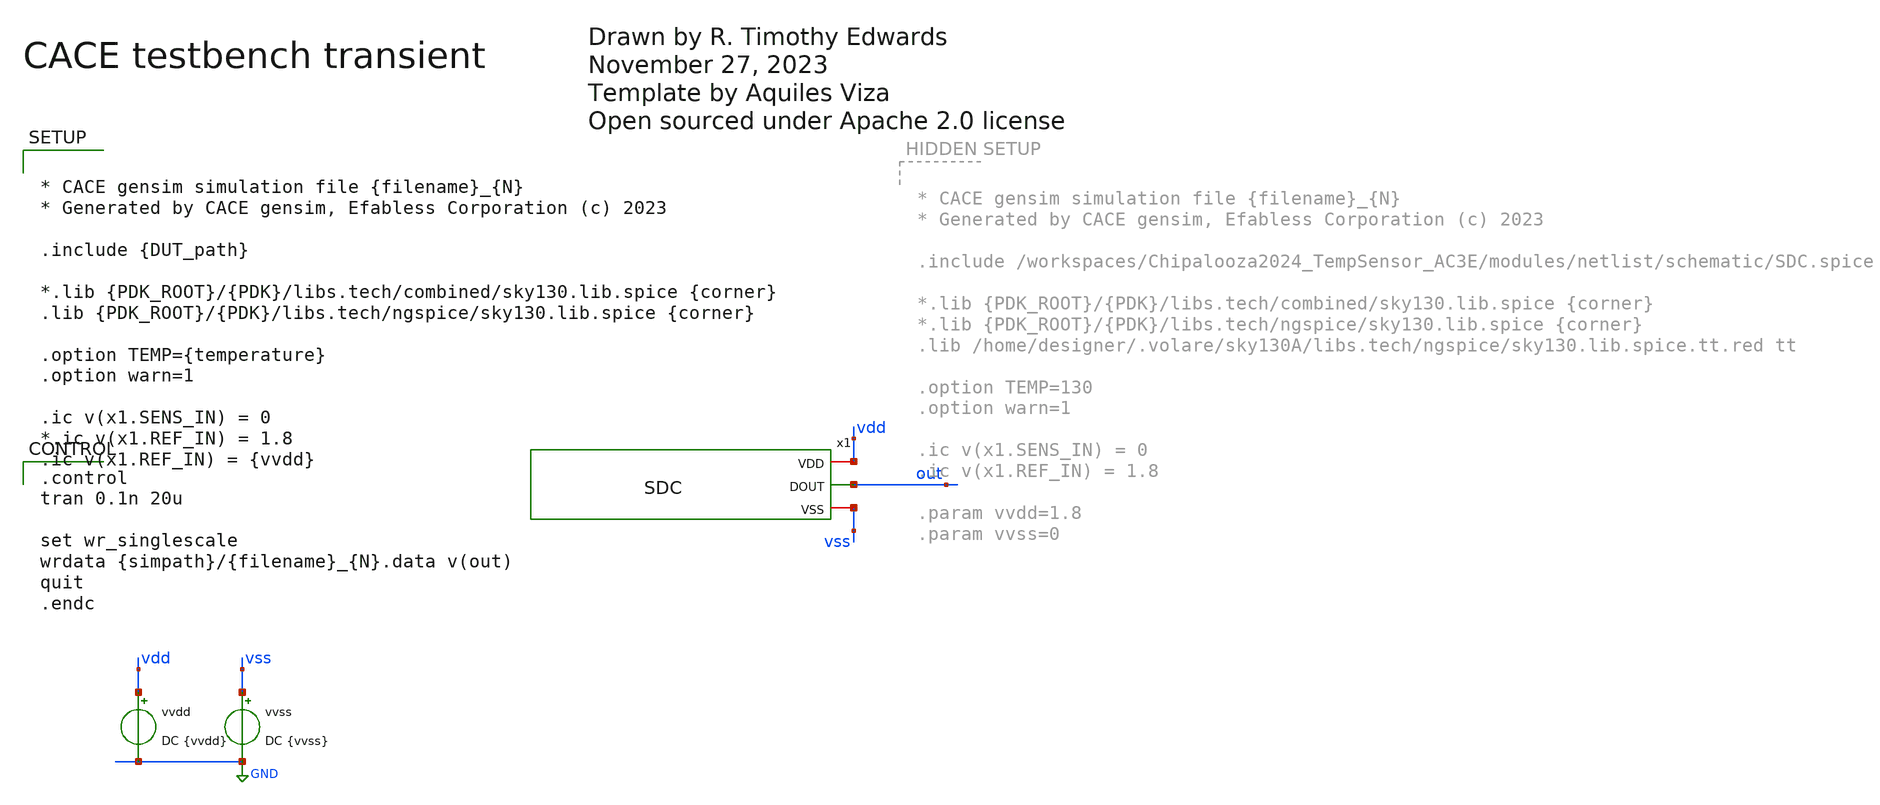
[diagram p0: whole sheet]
** sch_path: modules/cace/transient.sch
* Open sourced under Apache 2.0 license


* CACE gensim simulation file {filename}_{N}
* Generated by CACE gensim, Efabless Corporation (c) 2023

.include {DUT_path}

*.lib {PDK_ROOT}/{PDK}/libs.tech/combined/sky130.lib.spice {corner}
.lib {PDK_ROOT}/{PDK}/libs.tech/ngspice/sky130.lib.spice {corner}

.option TEMP={temperature}
.option warn=1

.ic v(x1.SENS_IN) = 0
*.ic v(x1.REF_IN) = 1.8
.ic v(x1.REF_IN) = {vvdd}


**.subckt transient
vvss vss GND DC {vvss}
vvdd vdd GND DC {vvdd}
x1 vdd out vss SDC
**** begin user architecture code

.control
tran 0.1n 20u

set wr_singlescale
wrdata {simpath}/{filename}_{N}.data v(out)
quit
.endc


**** end user architecture code
**.ends
.GLOBAL GND
.end
